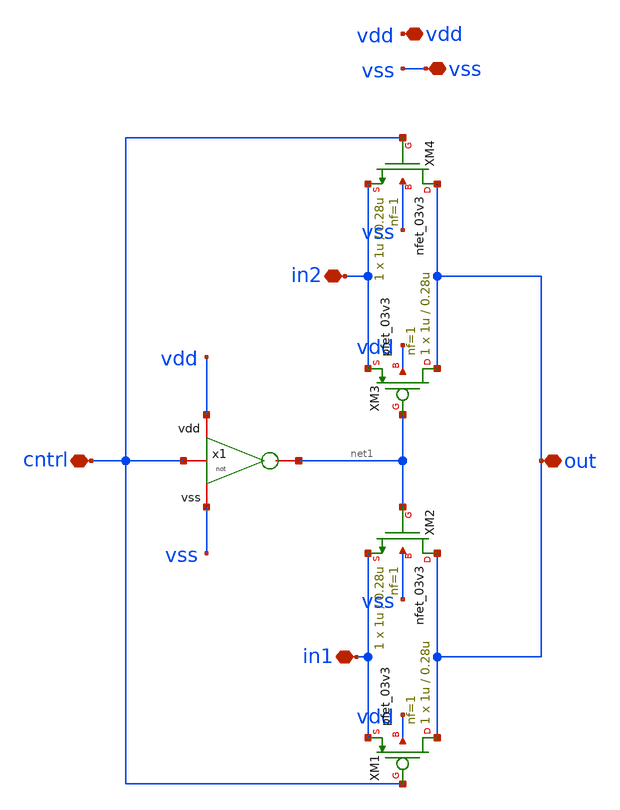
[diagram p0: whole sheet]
** sch_path: designs/libs/core_LIF_comp/core_conmutator/conmutator.sch
**.subckt conmutator vdd vss in2 out in1 cntrl
*.iopin vdd
*.iopin vss
*.iopin in2
*.iopin out
*.iopin in1
*.iopin cntrl
x1 vdd cntrl net1 vss not
XM3 out net1 in2 vdd pfet_03v3 L=0.28u W=1u nf=1 ad='int((nf+1)/2) * W/nf * 0.18u' as='int((nf+2)/2) * W/nf * 0.18u'
+ pd='2*int((nf+1)/2) * (W/nf + 0.18u)' ps='2*int((nf+2)/2) * (W/nf + 0.18u)' nrd='0.18u / W' nrs='0.18u / W'
+ sa=0 sb=0 sd=0 m=1
XM4 out cntrl in2 vss nfet_03v3 L=0.28u W=1u nf=1 ad='int((nf+1)/2) * W/nf * 0.18u' as='int((nf+2)/2) * W/nf * 0.18u'
+ pd='2*int((nf+1)/2) * (W/nf + 0.18u)' ps='2*int((nf+2)/2) * (W/nf + 0.18u)' nrd='0.18u / W' nrs='0.18u / W'
+ sa=0 sb=0 sd=0 m=1
XM1 out cntrl in1 vdd pfet_03v3 L=0.28u W=1u nf=1 ad='int((nf+1)/2) * W/nf * 0.18u' as='int((nf+2)/2) * W/nf * 0.18u'
+ pd='2*int((nf+1)/2) * (W/nf + 0.18u)' ps='2*int((nf+2)/2) * (W/nf + 0.18u)' nrd='0.18u / W' nrs='0.18u / W'
+ sa=0 sb=0 sd=0 m=1
XM2 out net1 in1 vss nfet_03v3 L=0.28u W=1u nf=1 ad='int((nf+1)/2) * W/nf * 0.18u' as='int((nf+2)/2) * W/nf * 0.18u'
+ pd='2*int((nf+1)/2) * (W/nf + 0.18u)' ps='2*int((nf+2)/2) * (W/nf + 0.18u)' nrd='0.18u / W' nrs='0.18u / W'
+ sa=0 sb=0 sd=0 m=1
**.ends

* expanding   symbol:  designs/libs/core_LIF_comp/core_not/not.sym # of pins=4
** sym_path: designs/libs/core_LIF_comp/core_not/not.sym
** sch_path: designs/libs/core_LIF_comp/core_not/not.sch
.subckt not vdd in out vss
*.iopin vdd
*.iopin vss
*.iopin in
*.iopin out
XM1 out in vdd vdd pfet_03v3 L=0.35u W=1u nf=1 ad='int((nf+1)/2) * W/nf * 0.18u' as='int((nf+2)/2) * W/nf * 0.18u'
+ pd='2*int((nf+1)/2) * (W/nf + 0.18u)' ps='2*int((nf+2)/2) * (W/nf + 0.18u)' nrd='0.18u / W' nrs='0.18u / W'
+ sa=0 sb=0 sd=0 m=1
XM3 out in vss vss nfet_03v3 L=0.28u W=1u nf=1 ad='int((nf+1)/2) * W/nf * 0.18u' as='int((nf+2)/2) * W/nf * 0.18u'
+ pd='2*int((nf+1)/2) * (W/nf + 0.18u)' ps='2*int((nf+2)/2) * (W/nf + 0.18u)' nrd='0.18u / W' nrs='0.18u / W'
+ sa=0 sb=0 sd=0 m=1
.ends

.end
